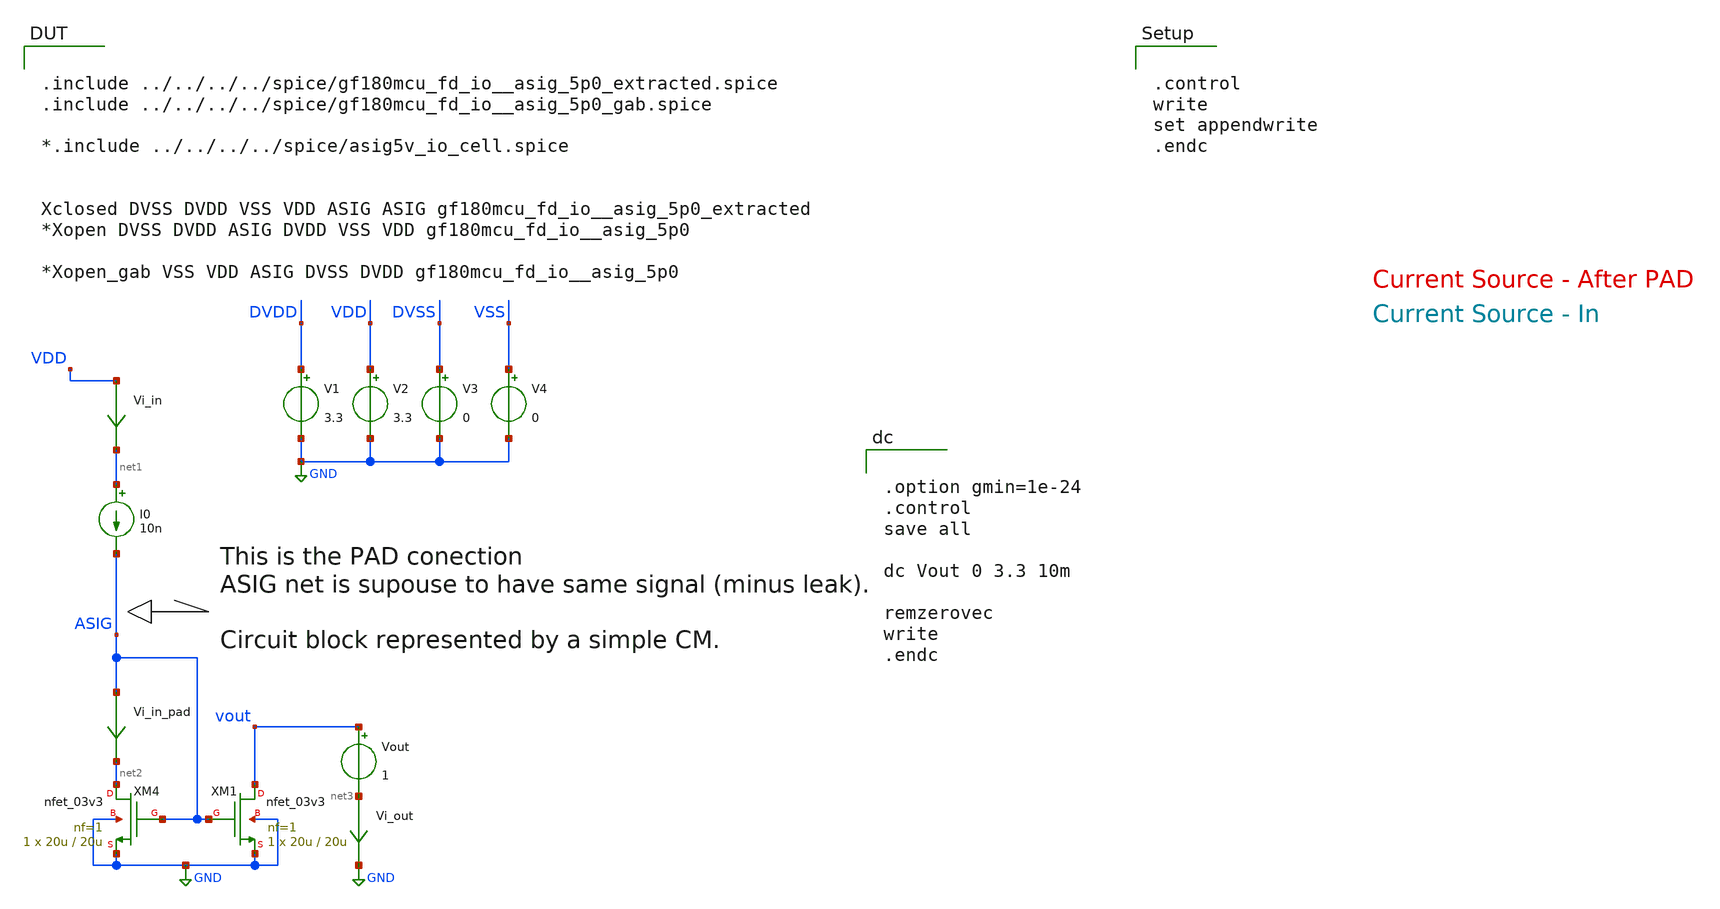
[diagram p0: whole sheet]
** sch_path: padframe/leakage_asig_5p0/test/leakage_asig_5p0.sch

.control
write
set appendwrite
.endc

.include $env(PDK_ROOT)/$env(PDK)/libs.tech/ngspice/design.ngspice
.lib $env(PDK_ROOT)/$env(PDK)/libs.tech/ngspice/sm141064.ngspice typical
.lib $env(PDK_ROOT)/$env(PDK)/libs.tech/ngspice/sm141064.ngspice diode_typical
.lib $env(PDK_ROOT)/$env(PDK)/libs.tech/ngspice/sm141064.ngspice res_typical
.lib $env(PDK_ROOT)/$env(PDK)/libs.tech/ngspice/sm141064.ngspice mimcap_typical
.lib $env(PDK_ROOT)/$env(PDK)/libs.tech/ngspice/sm141064.ngspice moscap_typical
.lib $env(PDK_ROOT)/$env(PDK)/libs.tech/ngspice/sm141064.ngspice bjt_typical
*.lib $env(PDK_ROOT)/$env(PDK)/libs.tech/ngspice/sm141064.ngspice cap_mim

**.subckt leakage_asig_5p0
V1 DVDD GND 3.3
V2 VDD GND 3.3
V3 DVSS GND 0
V4 VSS GND 0
XM1 vout ASIG GND GND nfet_03v3 L=20u W=20u nf=1 ad='int((nf+1)/2) * W/nf * 0.18u' as='int((nf+2)/2) * W/nf * 0.18u'
+ pd='2*int((nf+1)/2) * (W/nf + 0.18u)' ps='2*int((nf+2)/2) * (W/nf + 0.18u)' nrd='0.18u / W' nrs='0.18u / W'
+ sa=0 sb=0 sd=0 m=1
XM4 net2 ASIG GND GND nfet_03v3 L=20u W=20u nf=1 ad='int((nf+1)/2) * W/nf * 0.18u' as='int((nf+2)/2) * W/nf * 0.18u'
+ pd='2*int((nf+1)/2) * (W/nf + 0.18u)' ps='2*int((nf+2)/2) * (W/nf + 0.18u)' nrd='0.18u / W' nrs='0.18u / W'
+ sa=0 sb=0 sd=0 m=1
I0 net1 ASIG 10n
Vi_in VDD net1 0
.save i(vi_in)
Vi_in_pad ASIG net2 0
.save i(vi_in_pad)
Vi_out net3 GND 0
.save i(vi_out)
Vout vout net3 1
**** begin user architecture code


.option gmin=1e-24
.control
save all

dc Vout 0 3.3 10m

remzerovec
write
.endc


.include ../../../../spice/gf180mcu_fd_io__asig_5p0_extracted.spice
.include ../../../../spice/gf180mcu_fd_io__asig_5p0_gab.spice

*.include ../../../../spice/asig5v_io_cell.spice


Xclosed DVSS DVDD VSS VDD ASIG ASIG gf180mcu_fd_io__asig_5p0_extracted
*Xopen DVSS DVDD ASIG DVDD VSS VDD gf180mcu_fd_io__asig_5p0

*Xopen_gab VSS VDD ASIG DVSS DVDD gf180mcu_fd_io__asig_5p0


**** end user architecture code
**.ends
.GLOBAL GND
.end
